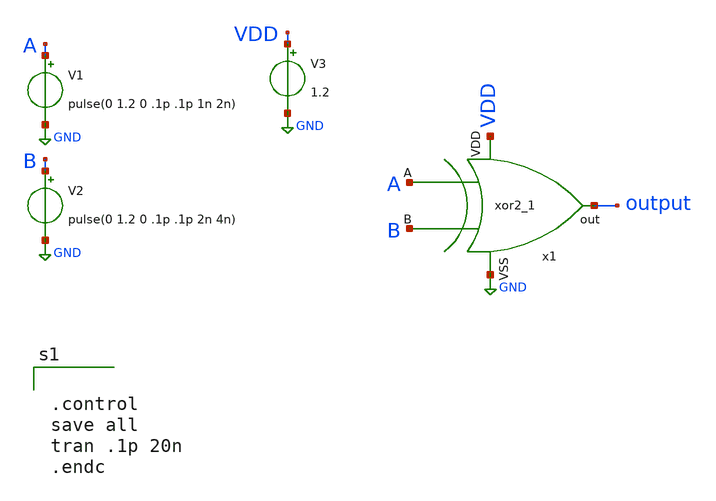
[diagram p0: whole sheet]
** sch_path: xor2/xor2_tb.sch
**.subckt xor2_tb
x1 A B VDD GND output xor2
V1 A GND pulse(0 1.2 0 .1p .1p 1n 2n)
V2 B GND pulse(0 1.2 0 .1p .1p 2n 4n)
V3 VDD GND 1.2
**** begin user architecture code

** opencircuitdesign pdks install
.lib $::SKYWATER_MODELS/sky130.lib.spice tt




.control
save all
tran .1p 20n
.endc

**** end user architecture code
**.ends

* expanding   symbol:  xor2.sym # of pins=5
** sym_path: xor2/xor2.sym
** sch_path: xor2/xor2.sch
.subckt xor2 A B VDD VSS out
*.ipin A
*.ipin B
*.opin out
*.ipin VDD
*.ipin VSS
XM1 out notA net3 net3 sky130_fd_pr__nfet_01v8 L=0.15 W=1 nf=1 ad='int((nf+1)/2) * W/nf * 0.29' as='int((nf+2)/2) * W/nf * 0.29'
+ pd='2*int((nf+1)/2) * (W/nf + 0.29)' ps='2*int((nf+2)/2) * (W/nf + 0.29)' nrd='0.29 / W' nrs='0.29 / W'
+ sa=0 sb=0 sd=0 mult=1 m=1
XM2 out B net1 net1 sky130_fd_pr__pfet_01v8 L=0.15 W=1 nf=1 ad='int((nf+1)/2) * W/nf * 0.29' as='int((nf+2)/2) * W/nf * 0.29'
+ pd='2*int((nf+1)/2) * (W/nf + 0.29)' ps='2*int((nf+2)/2) * (W/nf + 0.29)' nrd='0.29 / W' nrs='0.29 / W'
+ sa=0 sb=0 sd=0 mult=1 m=1
XM3 net3 notB VSS VSS sky130_fd_pr__nfet_01v8 L=0.15 W=1 nf=1 ad='int((nf+1)/2) * W/nf * 0.29' as='int((nf+2)/2) * W/nf * 0.29'
+ pd='2*int((nf+1)/2) * (W/nf + 0.29)' ps='2*int((nf+2)/2) * (W/nf + 0.29)' nrd='0.29 / W' nrs='0.29 / W'
+ sa=0 sb=0 sd=0 mult=1 m=1
XM4 net1 notA VDD VDD sky130_fd_pr__pfet_01v8 L=0.15 W=1 nf=1 ad='int((nf+1)/2) * W/nf * 0.29' as='int((nf+2)/2) * W/nf * 0.29'
+ pd='2*int((nf+1)/2) * (W/nf + 0.29)' ps='2*int((nf+2)/2) * (W/nf + 0.29)' nrd='0.29 / W' nrs='0.29 / W'
+ sa=0 sb=0 sd=0 mult=1 m=1
XM5 net4 A VDD VDD sky130_fd_pr__pfet_01v8 L=0.15 W=1 nf=1 ad='int((nf+1)/2) * W/nf * 0.29' as='int((nf+2)/2) * W/nf * 0.29'
+ pd='2*int((nf+1)/2) * (W/nf + 0.29)' ps='2*int((nf+2)/2) * (W/nf + 0.29)' nrd='0.29 / W' nrs='0.29 / W'
+ sa=0 sb=0 sd=0 mult=1 m=1
XM6 out notB net4 net4 sky130_fd_pr__pfet_01v8 L=0.15 W=1 nf=1 ad='int((nf+1)/2) * W/nf * 0.29' as='int((nf+2)/2) * W/nf * 0.29'
+ pd='2*int((nf+1)/2) * (W/nf + 0.29)' ps='2*int((nf+2)/2) * (W/nf + 0.29)' nrd='0.29 / W' nrs='0.29 / W'
+ sa=0 sb=0 sd=0 mult=1 m=1
XM7 out A net2 net2 sky130_fd_pr__nfet_01v8 L=0.15 W=1 nf=1 ad='int((nf+1)/2) * W/nf * 0.29' as='int((nf+2)/2) * W/nf * 0.29'
+ pd='2*int((nf+1)/2) * (W/nf + 0.29)' ps='2*int((nf+2)/2) * (W/nf + 0.29)' nrd='0.29 / W' nrs='0.29 / W'
+ sa=0 sb=0 sd=0 mult=1 m=1
XM8 net2 B VSS VSS sky130_fd_pr__nfet_01v8 L=0.15 W=1 nf=1 ad='int((nf+1)/2) * W/nf * 0.29' as='int((nf+2)/2) * W/nf * 0.29'
+ pd='2*int((nf+1)/2) * (W/nf + 0.29)' ps='2*int((nf+2)/2) * (W/nf + 0.29)' nrd='0.29 / W' nrs='0.29 / W'
+ sa=0 sb=0 sd=0 mult=1 m=1
XM9 notA A VDD VDD sky130_fd_pr__pfet_01v8 L=0.15 W=1 nf=1 ad='int((nf+1)/2) * W/nf * 0.29' as='int((nf+2)/2) * W/nf * 0.29'
+ pd='2*int((nf+1)/2) * (W/nf + 0.29)' ps='2*int((nf+2)/2) * (W/nf + 0.29)' nrd='0.29 / W' nrs='0.29 / W'
+ sa=0 sb=0 sd=0 mult=1 m=1
XM10 notA A VSS VSS sky130_fd_pr__nfet_01v8 L=0.15 W=1 nf=1 ad='int((nf+1)/2) * W/nf * 0.29' as='int((nf+2)/2) * W/nf * 0.29'
+ pd='2*int((nf+1)/2) * (W/nf + 0.29)' ps='2*int((nf+2)/2) * (W/nf + 0.29)' nrd='0.29 / W' nrs='0.29 / W'
+ sa=0 sb=0 sd=0 mult=1 m=1
XM11 notB B VDD VDD sky130_fd_pr__pfet_01v8 L=0.15 W=1 nf=1 ad='int((nf+1)/2) * W/nf * 0.29' as='int((nf+2)/2) * W/nf * 0.29'
+ pd='2*int((nf+1)/2) * (W/nf + 0.29)' ps='2*int((nf+2)/2) * (W/nf + 0.29)' nrd='0.29 / W' nrs='0.29 / W'
+ sa=0 sb=0 sd=0 mult=1 m=1
XM12 notB B VSS VSS sky130_fd_pr__nfet_01v8 L=0.15 W=1 nf=1 ad='int((nf+1)/2) * W/nf * 0.29' as='int((nf+2)/2) * W/nf * 0.29'
+ pd='2*int((nf+1)/2) * (W/nf + 0.29)' ps='2*int((nf+2)/2) * (W/nf + 0.29)' nrd='0.29 / W' nrs='0.29 / W'
+ sa=0 sb=0 sd=0 mult=1 m=1
.ends

.GLOBAL GND
.end
